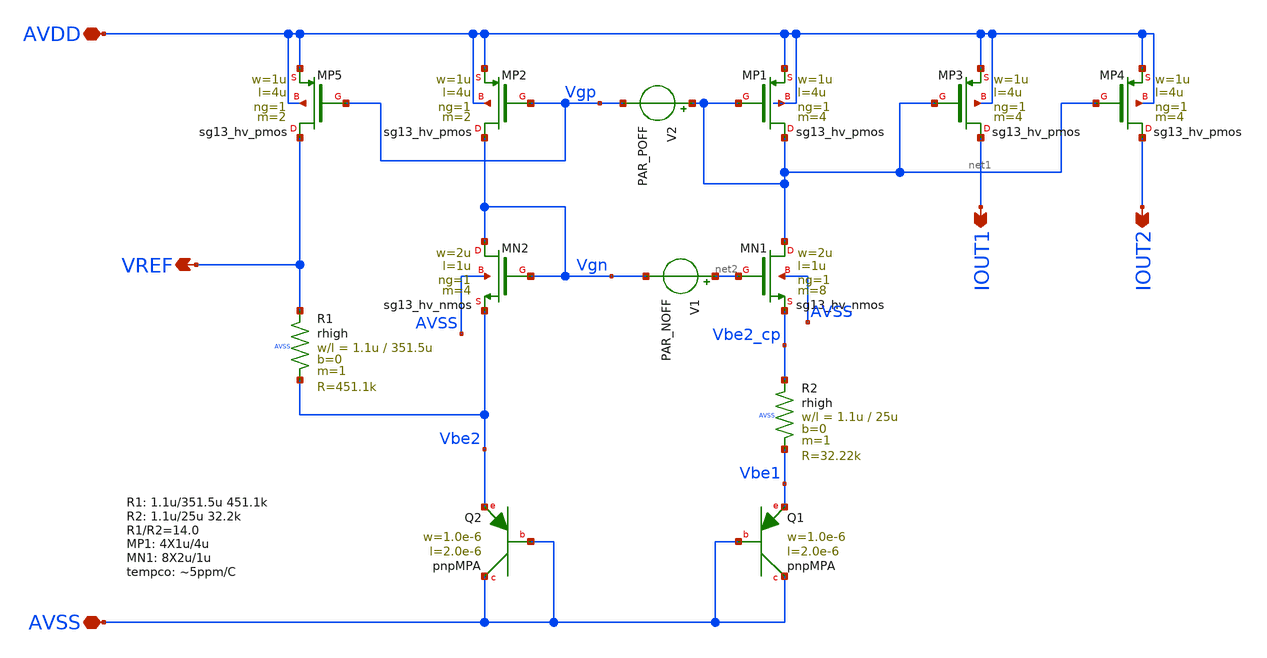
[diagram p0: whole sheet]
** sch_path: xschem/pmbgr1.sch
**.subckt pmbgr1 AVDD AVSS VREF IOUT1 IOUT2
*.iopin AVDD
*.iopin AVSS
*.opin VREF
*.opin IOUT1
*.opin IOUT2
XQ1 AVSS AVSS Vbe1 pnpMPA a=2p p=6u m=8
XQ2 AVSS AVSS Vbe2 pnpMPA a=2p p=6u m=1
XMN2 Vgn Vgn Vbe2 AVSS sg13_hv_nmos w=2u l=1u ng=1 m=4 mm_ok=1
XMN1 net1 net2 Vbe2_cp AVSS sg13_hv_nmos w=2u l=1u ng=1 m=8 mm_ok=1
XMP2 Vgn Vgp AVDD AVDD sg13_hv_pmos w=1u l=4u ng=1 m=2 mm_ok=1
XMP1 net1 net1 AVDD AVDD sg13_hv_pmos w=1u l=4u ng=1 m=4 mm_ok=1
XR2 Vbe2_cp Vbe1 AVSS rhigh w=1.1u l=25u m=1 b=0 mm_ok=1
XMP3 IOUT1 net1 AVDD AVDD sg13_hv_pmos w=1u l=4u ng=1 m=4 mm_ok=1
XMP4 IOUT2 net1 AVDD AVDD sg13_hv_pmos w=1u l=4u ng=1 m=4 mm_ok=1
XMP5 VREF Vgp AVDD AVDD sg13_hv_pmos w=1u l=4u ng=1 m=2 mm_ok=1
XR1 VREF Vbe2 AVSS rhigh w=1.1u l=351.5u m=1 b=0 mm_ok=1
V1 net2 Vgn PAR_NOFF
V2 net1 Vgp PAR_POFF
**.ends
.end
